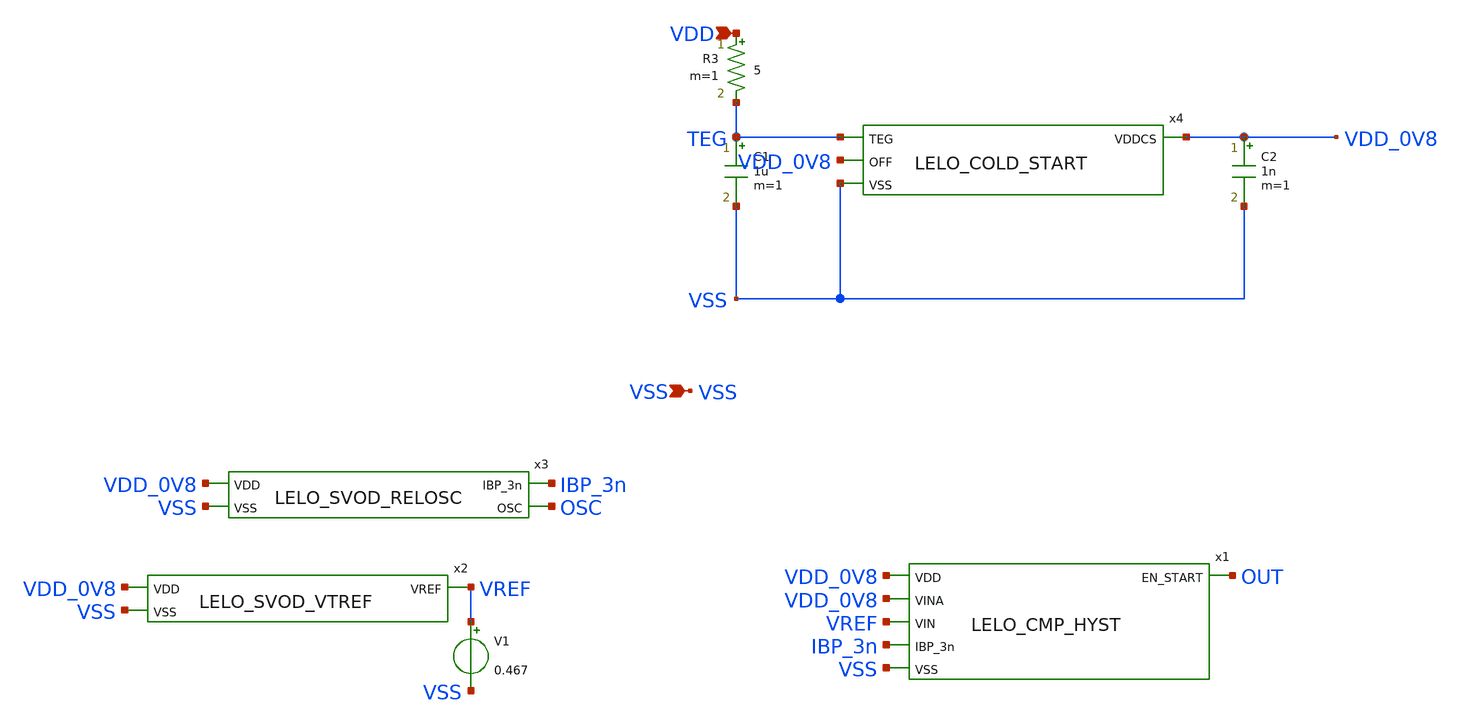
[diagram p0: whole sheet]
** sch_path: design/LELO_SVOD_SKY130A/LELO_STARTUP_DETECTOR_TEST.sch
**.subckt LELO_STARTUP_DETECTOR_TEST VSS VDD
*.ipin VSS
*.ipin VDD
x1 VDD_0V8 OUT VDD_0V8 VREF IBP_3n VSS LELO_CMP_HYST
x2 VDD_0V8 VSS VREF LELO_SVOD_VTREF
x3 VDD_0V8 VSS IBP_3n OSC LELO_SVOD_RELOSC
x4 TEG VDD_0V8 VDD_0V8 VSS LELO_COLD_START
R3 VDD TEG 5 m=1
C1 TEG VSS 1u m=1
C2 VDD_0V8 VSS 1n m=1
V1 VREF VSS 0.467
**.ends
.end
